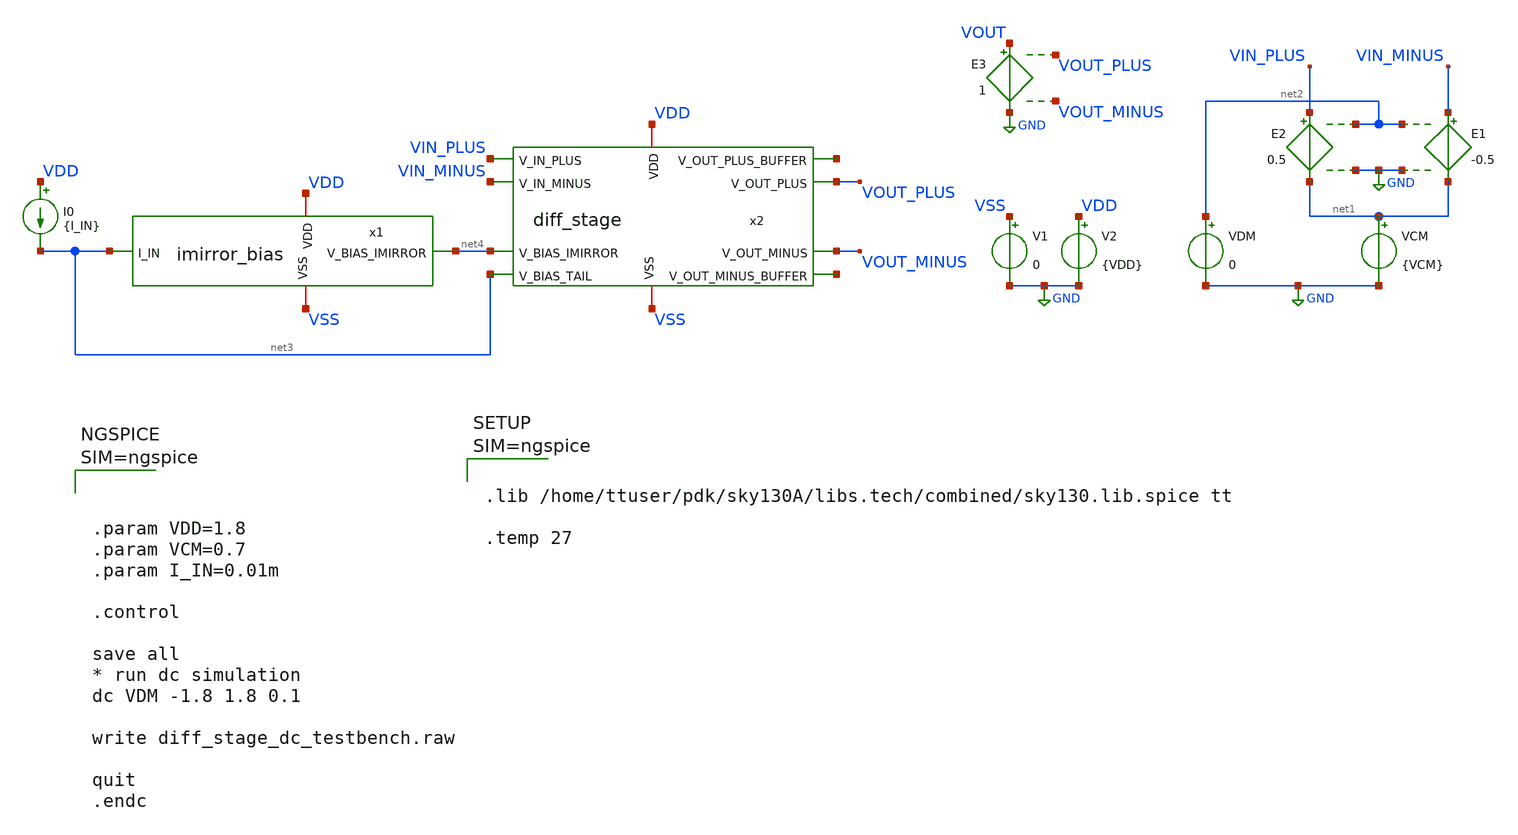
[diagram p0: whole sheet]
** sch_path: xschem/diff_stage_dc_testbench.sch
**.subckt diff_stage_dc_testbench
I0 VDD net3 {I_IN}
x1 VDD net4 net3 VSS imirror_bias
x2 VDD VSS VOUT_MINUS VOUT_PLUS net5 net6 VIN_PLUS VIN_MINUS net4 net3 diff_stage
V1 VSS GND 0
V2 VDD GND {VDD}
VDM net2 GND 0
VCM net1 GND {VCM}
E1 VIN_MINUS net1 net2 GND -0.5
E2 VIN_PLUS net1 net2 GND 0.5
E3 VOUT GND VOUT_PLUS VOUT_MINUS 1
**** begin user architecture code




.param VDD=1.8
.param VCM=0.7
.param I_IN=0.01m

.control

save all
* run dc simulation
dc VDM -1.8 1.8 0.1

write diff_stage_dc_testbench.raw

quit
.endc






.lib /home/ttuser/pdk/sky130A/libs.tech/combined/sky130.lib.spice tt

.temp 27



**** end user architecture code
**.ends

* expanding   symbol:  imirror_bias.sym # of pins=4
** sym_path: xschem/imirror_bias.sym
** sch_path: xschem/imirror_bias.sch
.subckt imirror_bias VDD V_BIAS_IMIRROR I_IN VSS
*.iopin VDD
*.iopin VSS
*.opin V_BIAS_IMIRROR
*.ipin I_IN
XM1 I_IN I_IN VSS VSS sky130_fd_pr__nfet_01v8 L=2 W=4 nf=2 ad='int((nf+1)/2) * W/nf * 0.29' as='int((nf+2)/2) * W/nf * 0.29'
+ pd='2*int((nf+1)/2) * (W/nf + 0.29)' ps='2*int((nf+2)/2) * (W/nf + 0.29)' nrd='0.29 / W' nrs='0.29 / W'
+ sa=0 sb=0 sd=0 mult=1 m=1
XM2 V_BIAS_IMIRROR I_IN VSS VSS sky130_fd_pr__nfet_01v8 L=2 W=4 nf=1 ad='int((nf+1)/2) * W/nf * 0.29'
+ as='int((nf+2)/2) * W/nf * 0.29' pd='2*int((nf+1)/2) * (W/nf + 0.29)' ps='2*int((nf+2)/2) * (W/nf + 0.29)'
+ nrd='0.29 / W' nrs='0.29 / W' sa=0 sb=0 sd=0 mult=1 m=1
XM3 V_BIAS_IMIRROR V_BIAS_IMIRROR VDD VDD sky130_fd_pr__pfet_01v8 L=0.25 W=4 nf=1 ad='int((nf+1)/2) * W/nf * 0.29'
+ as='int((nf+2)/2) * W/nf * 0.29' pd='2*int((nf+1)/2) * (W/nf + 0.29)' ps='2*int((nf+2)/2) * (W/nf + 0.29)'
+ nrd='0.29 / W' nrs='0.29 / W' sa=0 sb=0 sd=0 mult=1 m=1
.ends


* expanding   symbol:  diff_stage.sym # of pins=10
** sym_path: xschem/diff_stage.sym
** sch_path: xschem/diff_stage.sch
.subckt diff_stage VDD VSS V_OUT_MINUS V_OUT_PLUS V_OUT_MINUS_BUFFER V_OUT_PLUS_BUFFER V_IN_PLUS
+ V_IN_MINUS V_BIAS_IMIRROR V_BIAS_TAIL
*.opin V_OUT_PLUS
*.opin V_OUT_PLUS_BUFFER
*.opin V_OUT_MINUS
*.opin V_OUT_MINUS_BUFFER
*.ipin V_BIAS_IMIRROR
*.ipin V_IN_MINUS
*.ipin V_IN_PLUS
*.ipin V_BIAS_TAIL
*.iopin VDD
*.iopin VSS
x1 VDD V_OUT_MINUS V_BIAS_IMIRROR V_OUT_PLUS V_OUT_PLUS_BUFFER V_IN_MINUS VSS V_DRAIN_TAIL
+ diff_stage_half
x2 VDD V_OUT_PLUS V_BIAS_IMIRROR V_OUT_MINUS V_OUT_MINUS_BUFFER V_IN_PLUS VSS V_DRAIN_TAIL
+ diff_stage_half
XM1 V_DRAIN_TAIL V_BIAS_TAIL VSS VSS sky130_fd_pr__nfet_01v8 L=2 W=4 nf=2 ad='int((nf+1)/2) * W/nf * 0.29'
+ as='int((nf+2)/2) * W/nf * 0.29' pd='2*int((nf+1)/2) * (W/nf + 0.29)' ps='2*int((nf+2)/2) * (W/nf + 0.29)'
+ nrd='0.29 / W' nrs='0.29 / W' sa=0 sb=0 sd=0 mult=1 m=1
.ends


* expanding   symbol:  diff_stage_half.sym # of pins=8
** sym_path: xschem/diff_stage_half.sym
** sch_path: xschem/diff_stage_half.sch
.subckt diff_stage_half VDD V_FB_CROSSCOUPLED V_BIAS_IMIRROR V_OUT_DIFF V_OUT_DIFF_BUFFER V_IN_RING
+ VSS V_DRAIN_TAIL
*.ipin V_BIAS_IMIRROR
*.ipin V_FB_CROSSCOUPLED
*.ipin V_IN_RING
*.opin V_OUT_DIFF
*.iopin VDD
*.iopin VSS
*.opin V_OUT_DIFF_BUFFER
*.iopin V_DRAIN_TAIL
XM1 V_OUT_DIFF V_BIAS_IMIRROR VDD VDD sky130_fd_pr__pfet_01v8 L=2 W=4 nf=2 ad='int((nf+1)/2) * W/nf * 0.29'
+ as='int((nf+2)/2) * W/nf * 0.29' pd='2*int((nf+1)/2) * (W/nf + 0.29)' ps='2*int((nf+2)/2) * (W/nf + 0.29)'
+ nrd='0.29 / W' nrs='0.29 / W' sa=0 sb=0 sd=0 mult=1 m=1
XM2 V_OUT_DIFF V_FB_CROSSCOUPLED VDD VDD sky130_fd_pr__pfet_01v8 L=2 W=4 nf=2 ad='int((nf+1)/2) * W/nf * 0.29'
+ as='int((nf+2)/2) * W/nf * 0.29' pd='2*int((nf+1)/2) * (W/nf + 0.29)' ps='2*int((nf+2)/2) * (W/nf + 0.29)'
+ nrd='0.29 / W' nrs='0.29 / W' sa=0 sb=0 sd=0 mult=1 m=1
XM3 V_OUT_DIFF V_IN_RING V_DRAIN_TAIL VSS sky130_fd_pr__nfet_01v8 L=2 W=4 nf=2 ad='int((nf+1)/2) * W/nf * 0.29'
+ as='int((nf+2)/2) * W/nf * 0.29' pd='2*int((nf+1)/2) * (W/nf + 0.29)' ps='2*int((nf+2)/2) * (W/nf + 0.29)'
+ nrd='0.29 / W' nrs='0.29 / W' sa=0 sb=0 sd=0 mult=1 m=1
XM4 VSS V_OUT_DIFF VSS VSS sky130_fd_pr__nfet_01v8 L=11 W=11 nf=1 ad='int((nf+1)/2) * W/nf * 0.29' as='int((nf+2)/2) * W/nf * 0.29'
+ pd='2*int((nf+1)/2) * (W/nf + 0.29)' ps='2*int((nf+2)/2) * (W/nf + 0.29)' nrd='0.29 / W' nrs='0.29 / W'
+ sa=0 sb=0 sd=0 mult=1 m=1
x1 VDD VSS V_OUT_DIFF_BUFFER V_OUT_DIFF min_buffer
.ends


* expanding   symbol:  min_buffer.sym # of pins=4
** sym_path: xschem/min_buffer.sym
** sch_path: xschem/min_buffer.sch
.subckt min_buffer VDD VSS VOUT_BUFFER VIN_BUFFER
*.ipin VIN_BUFFER
*.opin VOUT_BUFFER
*.iopin VDD
*.iopin VSS
x1 VDD VSS VOUT_BUFFER INT_BUFFER min_inv
x2 VDD VSS INT_BUFFER VIN_BUFFER min_inv
.ends


* expanding   symbol:  min_inv.sym # of pins=4
** sym_path: xschem/min_inv.sym
** sch_path: xschem/min_inv.sch
.subckt min_inv VDD VSS VOUT_INV VIN_INV
*.iopin VDD
*.iopin VSS
*.ipin VIN_INV
*.opin VOUT_INV
XM2 VOUT_INV VIN_INV VSS VSS sky130_fd_pr__nfet_01v8 L=0.15 W=1 nf=1 ad='int((nf+1)/2) * W/nf * 0.29'
+ as='int((nf+2)/2) * W/nf * 0.29' pd='2*int((nf+1)/2) * (W/nf + 0.29)' ps='2*int((nf+2)/2) * (W/nf + 0.29)'
+ nrd='0.29 / W' nrs='0.29 / W' sa=0 sb=0 sd=0 mult=1 m=1
XM3 VOUT_INV VIN_INV VDD VDD sky130_fd_pr__pfet_01v8 L=0.15 W=1 nf=1 ad='int((nf+1)/2) * W/nf * 0.29'
+ as='int((nf+2)/2) * W/nf * 0.29' pd='2*int((nf+1)/2) * (W/nf + 0.29)' ps='2*int((nf+2)/2) * (W/nf + 0.29)'
+ nrd='0.29 / W' nrs='0.29 / W' sa=0 sb=0 sd=0 mult=1 m=1
.ends

.GLOBAL GND
.end
